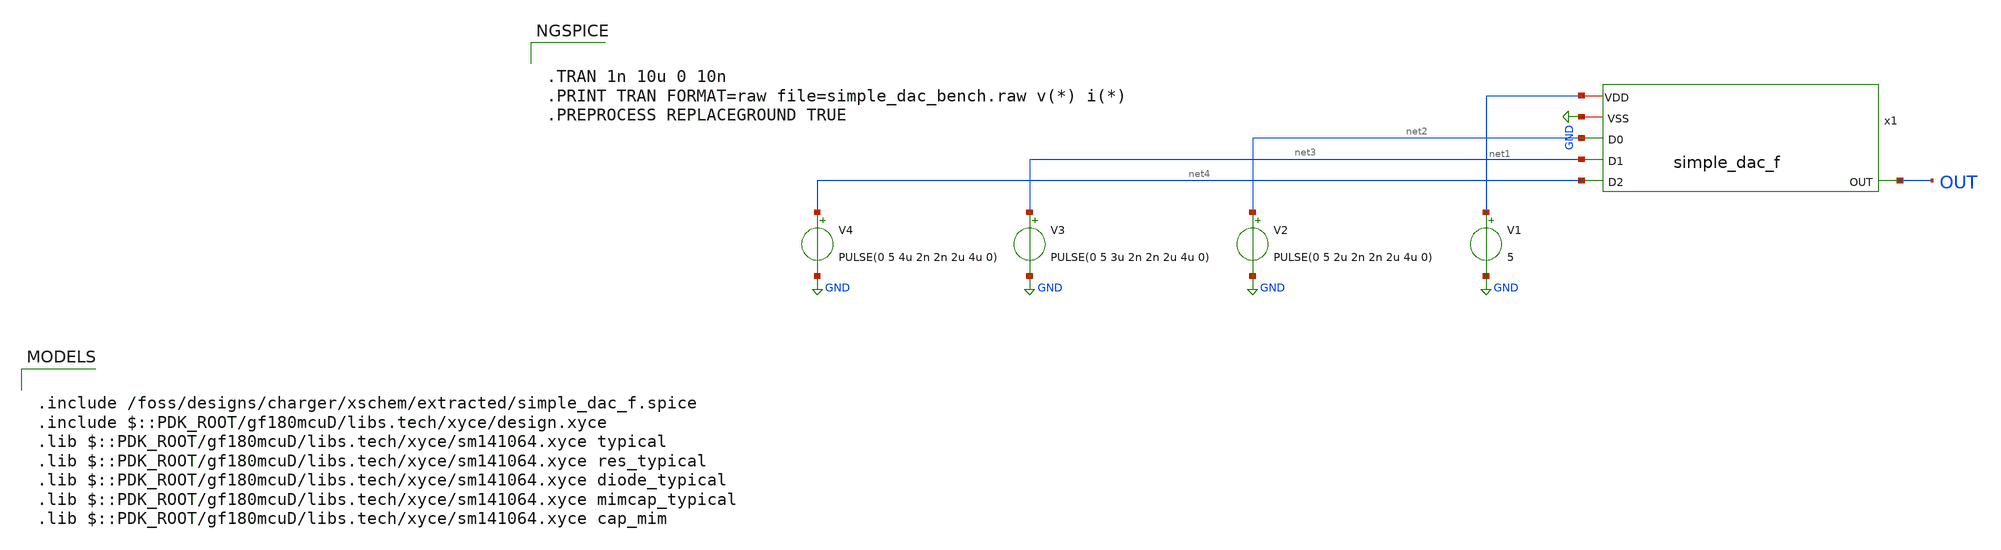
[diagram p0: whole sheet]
** sch_path: analog/xschem/simple_dac_bench.sch
**.subckt simple_dac_bench
V1 net1 GND 5
V2 net2 GND PULSE(0 5 2u 2n 2n 2u 4u 0)
V3 net3 GND PULSE(0 5 3u 2n 2n 2u 4u 0)
V4 net4 GND PULSE(0 5 4u 2n 2n 2u 4u 0)
x1 net1 GND net2 net3 net4 OUT simple_dac_f
**** begin user architecture code


.TRAN 1n 10u 0 10n
.PRINT TRAN FORMAT=raw file=simple_dac_bench.raw v(*) i(*)
.PREPROCESS REPLACEGROUND TRUE



.include /foss/designs/charger/xschem/extracted/simple_dac_f.spice
.include $::PDK_ROOT/gf180mcuD/libs.tech/xyce/design.xyce
.lib $::PDK_ROOT/gf180mcuD/libs.tech/xyce/sm141064.xyce typical
.lib $::PDK_ROOT/gf180mcuD/libs.tech/xyce/sm141064.xyce res_typical
.lib $::PDK_ROOT/gf180mcuD/libs.tech/xyce/sm141064.xyce diode_typical
.lib $::PDK_ROOT/gf180mcuD/libs.tech/xyce/sm141064.xyce mimcap_typical
.lib $::PDK_ROOT/gf180mcuD/libs.tech/xyce/sm141064.xyce cap_mim

**** end user architecture code
**.ends
.GLOBAL GND
.end
